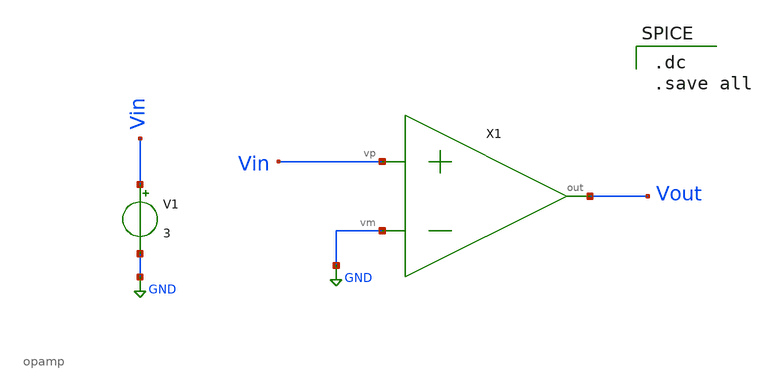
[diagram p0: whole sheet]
** sch_path: xschem/untitled.sch
**.subckt untitled
X1 Vin GND Vout opamp
V1 Vin GND 3
**** begin user architecture code

.dc
.save all

**** end user architecture code
**.ends

* expanding   symbol:  opamp.sym # of pins=3
** sym_path: xschem/MISC/opamp.sym
** sch_path: xschem/MISC/opamp.sch
.subckt opamp vp vm out
*.ipin vp
*.ipin vm
*.opin out
E1 out GND vp vm 1E6
.ends

.GLOBAL GND
.end
